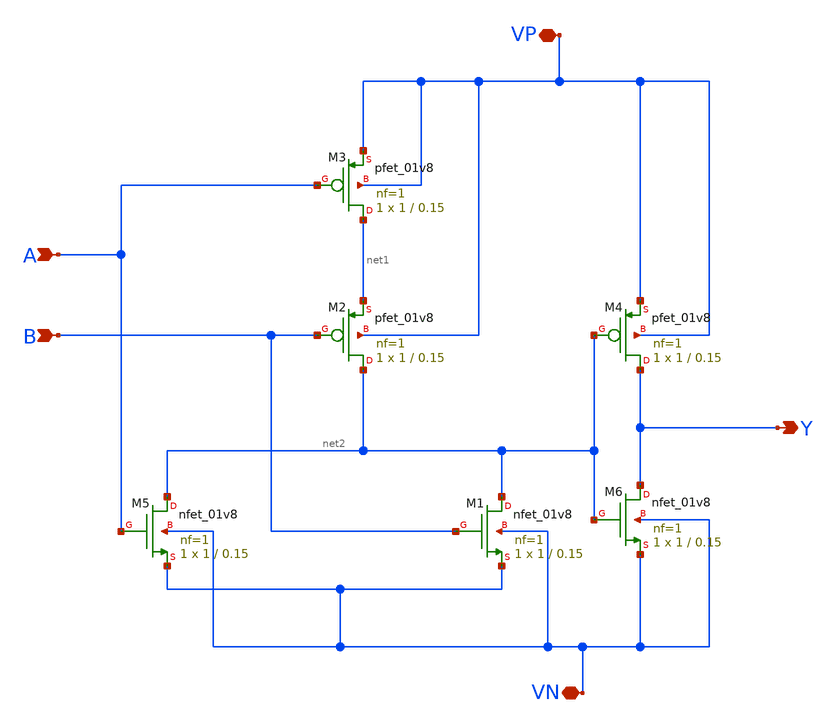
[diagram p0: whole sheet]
** sch_path: or.sch
**.subckt or Y VP VN B A
*.opin Y
*.iopin VP
*.iopin VN
*.ipin B
*.ipin A
XM5 net2 A VN VN sky130_fd_pr__nfet_01v8 L=0.15 W=1 nf=1 ad='int((nf+1)/2) * W/nf * 0.29' as='int((nf+2)/2) * W/nf * 0.29'
+ pd='2*int((nf+1)/2) * (W/nf + 0.29)' ps='2*int((nf+2)/2) * (W/nf + 0.29)' nrd='0.29 / W' nrs='0.29 / W'
+ sa=0 sb=0 sd=0 mult=1 m=1
XM1 net2 B VN VN sky130_fd_pr__nfet_01v8 L=0.15 W=1 nf=1 ad='int((nf+1)/2) * W/nf * 0.29' as='int((nf+2)/2) * W/nf * 0.29'
+ pd='2*int((nf+1)/2) * (W/nf + 0.29)' ps='2*int((nf+2)/2) * (W/nf + 0.29)' nrd='0.29 / W' nrs='0.29 / W'
+ sa=0 sb=0 sd=0 mult=1 m=1
XM2 net2 B net1 VP sky130_fd_pr__pfet_01v8 L=0.15 W=1 nf=1 ad='int((nf+1)/2) * W/nf * 0.29' as='int((nf+2)/2) * W/nf * 0.29'
+ pd='2*int((nf+1)/2) * (W/nf + 0.29)' ps='2*int((nf+2)/2) * (W/nf + 0.29)' nrd='0.29 / W' nrs='0.29 / W'
+ sa=0 sb=0 sd=0 mult=1 m=1
XM3 net1 A VP VP sky130_fd_pr__pfet_01v8 L=0.15 W=1 nf=1 ad='int((nf+1)/2) * W/nf * 0.29' as='int((nf+2)/2) * W/nf * 0.29'
+ pd='2*int((nf+1)/2) * (W/nf + 0.29)' ps='2*int((nf+2)/2) * (W/nf + 0.29)' nrd='0.29 / W' nrs='0.29 / W'
+ sa=0 sb=0 sd=0 mult=1 m=1
XM4 Y net2 VP VP sky130_fd_pr__pfet_01v8 L=0.15 W=1 nf=1 ad='int((nf+1)/2) * W/nf * 0.29' as='int((nf+2)/2) * W/nf * 0.29'
+ pd='2*int((nf+1)/2) * (W/nf + 0.29)' ps='2*int((nf+2)/2) * (W/nf + 0.29)' nrd='0.29 / W' nrs='0.29 / W'
+ sa=0 sb=0 sd=0 mult=1 m=1
XM6 Y net2 VN VN sky130_fd_pr__nfet_01v8 L=0.15 W=1 nf=1 ad='int((nf+1)/2) * W/nf * 0.29' as='int((nf+2)/2) * W/nf * 0.29'
+ pd='2*int((nf+1)/2) * (W/nf + 0.29)' ps='2*int((nf+2)/2) * (W/nf + 0.29)' nrd='0.29 / W' nrs='0.29 / W'
+ sa=0 sb=0 sd=0 mult=1 m=1
**.ends
.end
